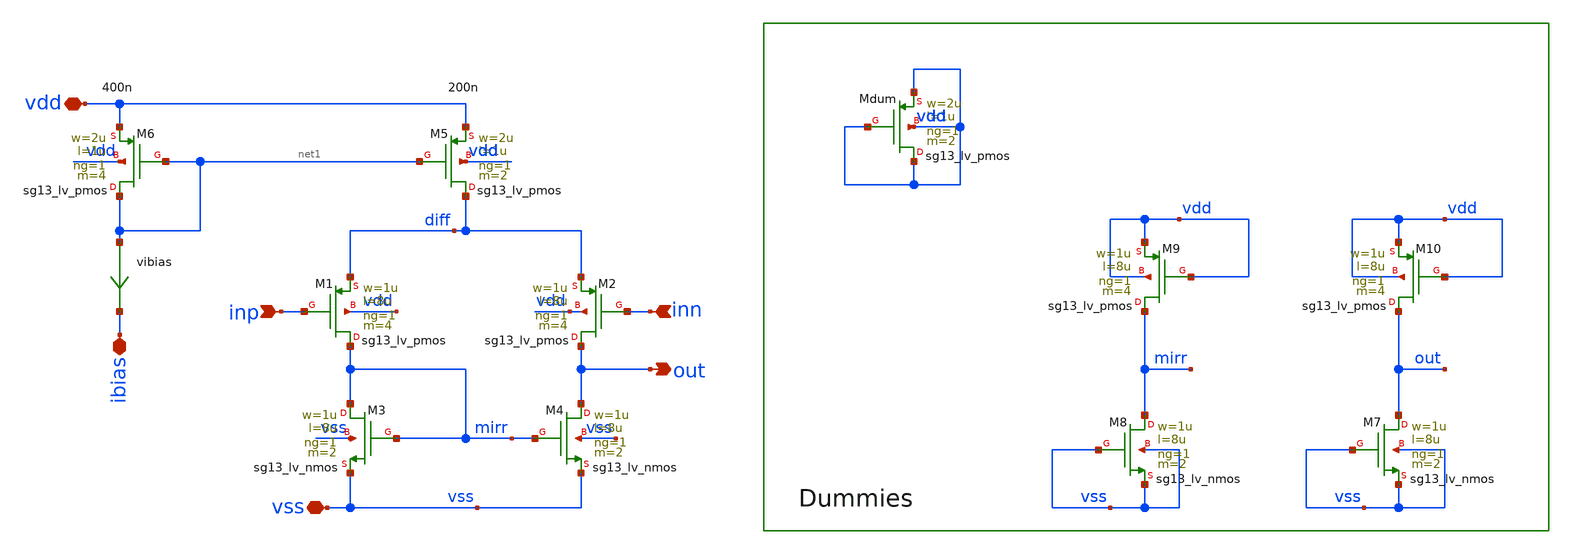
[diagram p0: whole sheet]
** sch_path: xschem/bandgap_orig/bandgap_amp.sch
**.subckt bandgap_amp out inp inn vdd vss ibias
*.opin out
*.ipin inp
*.ipin inn
*.iopin vdd
*.iopin vss
*.iopin ibias
vibias net1 ibias 0
.save i(vibias)
XM4 out mirr vss vss sg13_lv_nmos w=1u l=8u ng=1 m=2 mm_ok=1
XM3 mirr mirr vss vss sg13_lv_nmos w=1u l=8u ng=1 m=2 mm_ok=1
XM1 mirr inp diff vdd sg13_lv_pmos w=1u l=8u ng=1 m=4 mm_ok=1
XM2 out inn diff vdd sg13_lv_pmos w=1u l=8u ng=1 m=4 mm_ok=1
XM5 diff net1 vdd vdd sg13_lv_pmos w=2u l=1u ng=1 m=2 mm_ok=1
XM6 net1 net1 vdd vdd sg13_lv_pmos w=2u l=1u ng=1 m=4 mm_ok=1
XMdum vdd vdd vdd vdd sg13_lv_pmos w=2u l=1u ng=1 m=2 mm_ok=1
XM7 out vss vss vss sg13_lv_nmos w=1u l=8u ng=1 m=2 mm_ok=1
XM8 mirr vss vss vss sg13_lv_nmos w=1u l=8u ng=1 m=2 mm_ok=1
XM9 mirr vdd vdd vdd sg13_lv_pmos w=1u l=8u ng=1 m=4 mm_ok=1
XM10 out vdd vdd vdd sg13_lv_pmos w=1u l=8u ng=1 m=4 mm_ok=1
**.ends
.end
